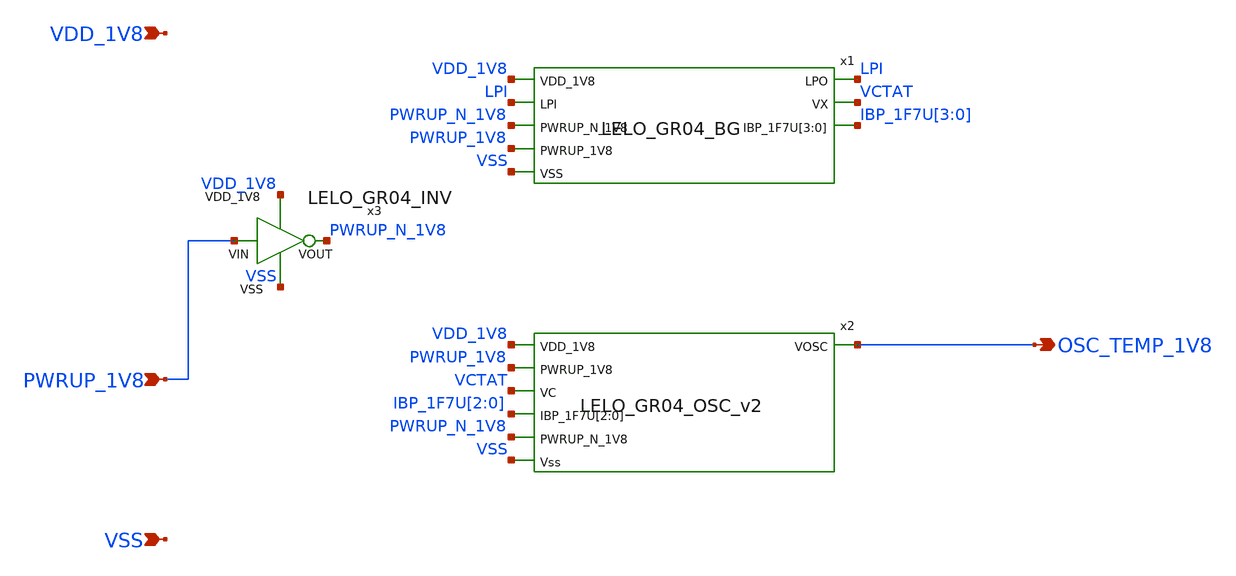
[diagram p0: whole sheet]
** sch_path: design/LELO_GR04_SKY130A/LELO_GR04.sch
**.subckt LELO_GR04 VDD_1V8 VSS PWRUP_1V8 OSC_TEMP_1V8
*.ipin VDD_1V8
*.ipin VSS
*.ipin PWRUP_1V8
*.opin OSC_TEMP_1V8
x1 VDD_1V8 LPI LPI VCTAT PWRUP_N_1V8 IBP_1F7U[3] IBP_1F7U[2] IBP_1F7U[1] IBP_1F7U[0] PWRUP_1V8 VSS
+ LELO_GR04_BG
x2 VDD_1V8 PWRUP_1V8 VCTAT IBP_1F7U[2] IBP_1F7U[1] IBP_1F7U[0] PWRUP_N_1V8 VSS OSC_TEMP_1V8
+ LELO_GR04_OSC_v2
x3 VDD_1V8 PWRUP_1V8 PWRUP_N_1V8 VSS LELO_GR04_INV
**.ends
.end
